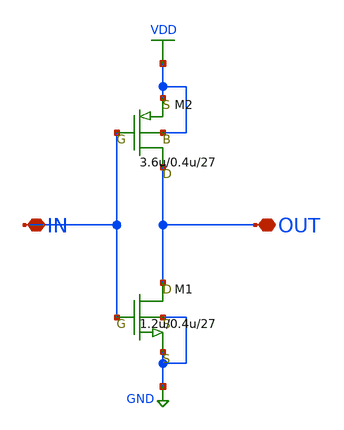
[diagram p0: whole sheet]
** sch_path: LR_hasegawa/LR_Work2/Citizen035/INVERTER27_Citizen.sch
**.subckt INVERTER27_Citizen IN OUT
*.iopin IN
*.iopin OUT
M1 OUT IN GND GND nch w=1.2u l=0.4u as=0 ps=0 ad=0 pd=0 m=27
M2 OUT IN VDD VDD pch w=3.6u l=0.4u as=0 ps=0 ad=0 pd=0 m=27
**.ends
.GLOBAL VDD
.GLOBAL GND
.end
